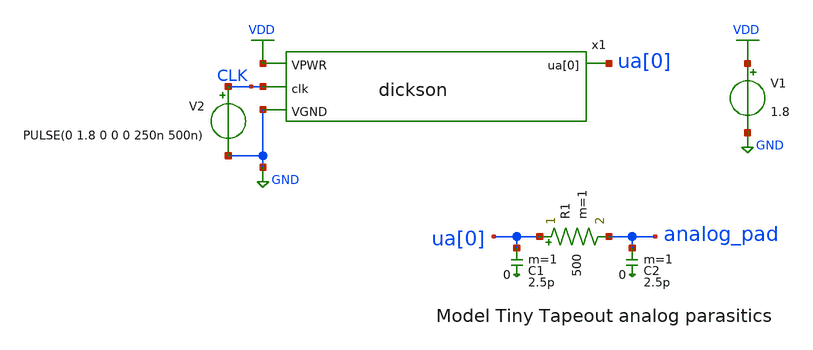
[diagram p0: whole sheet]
** sch_path: xschem/testbench.sch
**.subckt testbench
x1 VDD CLK ua[0] GND dickson
V1 VDD GND 1.8
V2 CLK GND PULSE(0 1.8 0 0 0 250n 500n)
R1 ua[0] analog_pad 500 m=1
C1 ua[0] 0 2.5p m=1
C2 analog_pad 0 2.5p m=1
**** begin user architecture code

** opencircuitdesign pdks install
.lib $::SKYWATER_MODELS/sky130.lib.spice tt





.tran 10n 100u
.save all

.control
run
write testbench.raw
.endc


**** end user architecture code
**.ends
.GLOBAL GND
.GLOBAL VDD
.end
